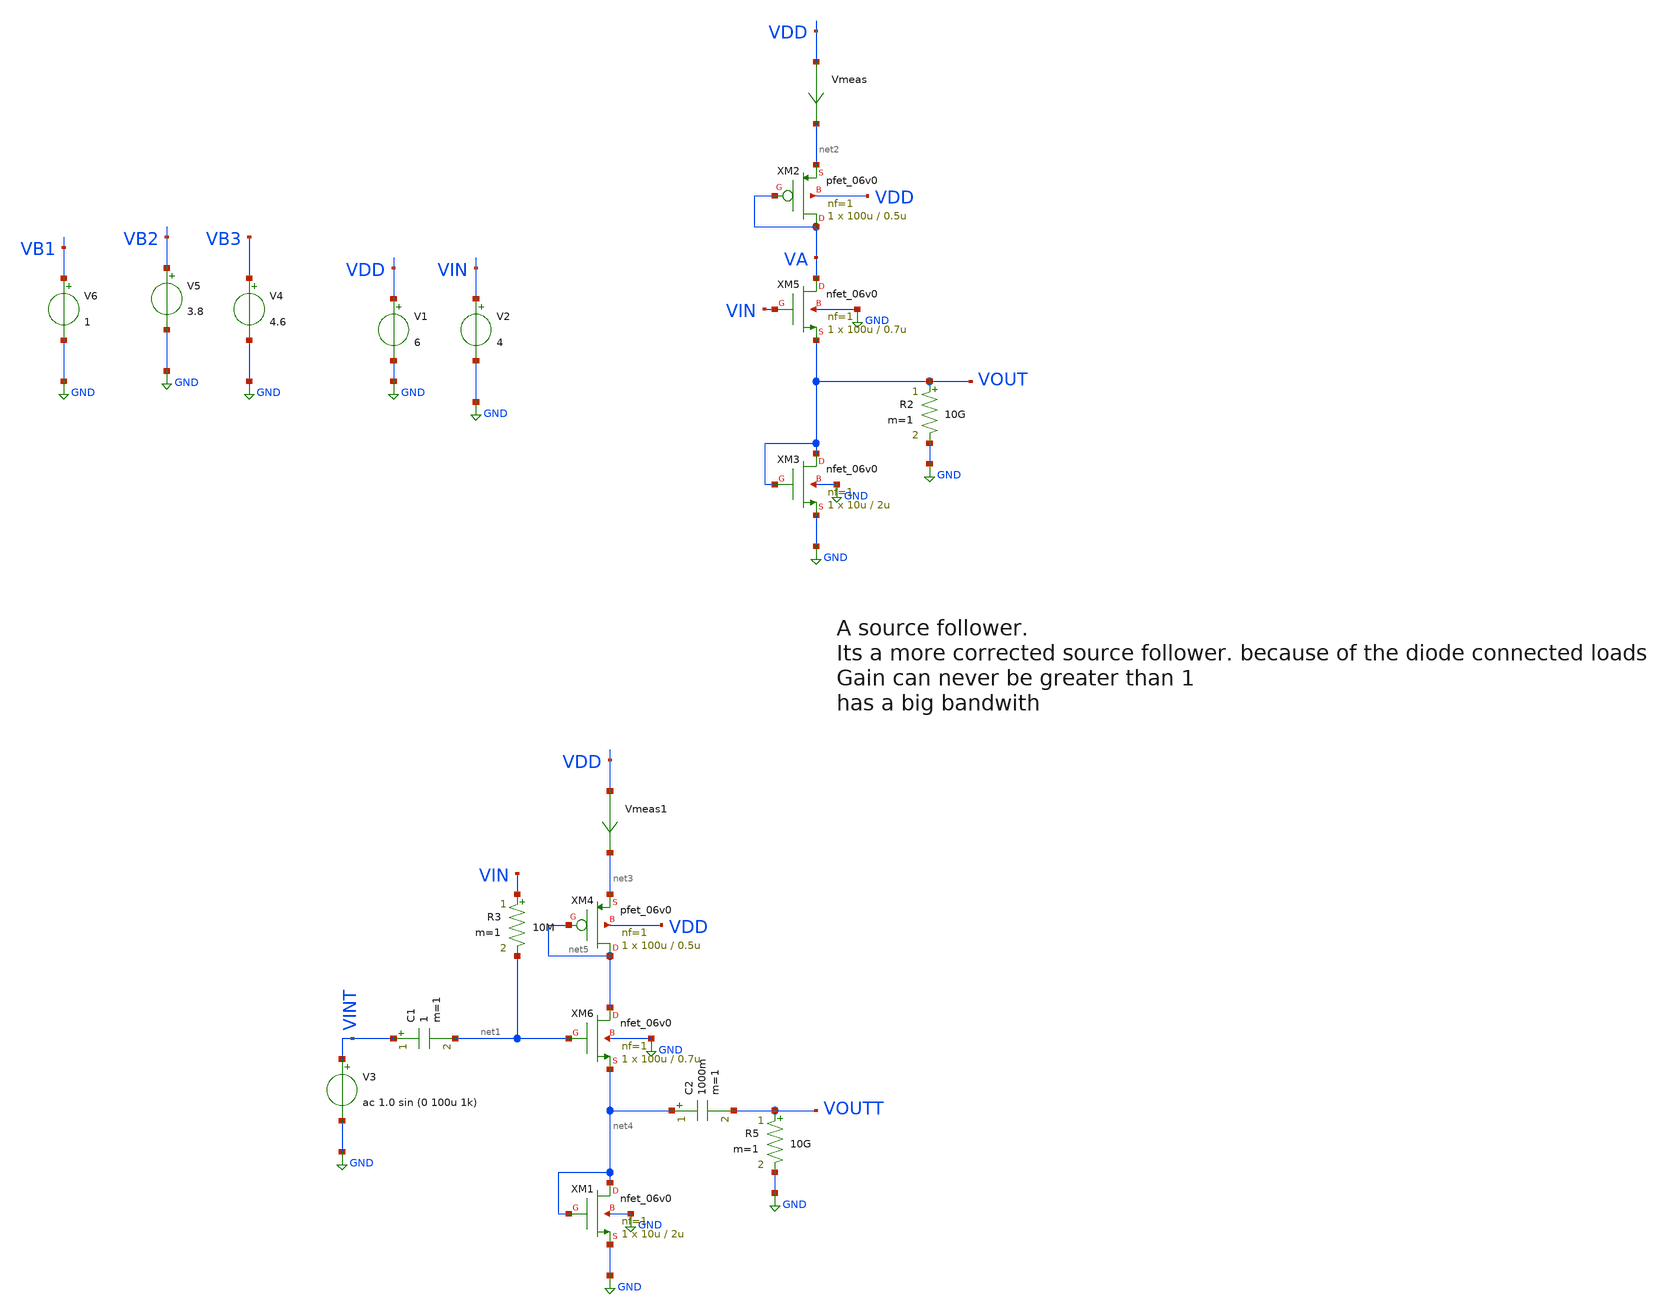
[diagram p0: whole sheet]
** sch_path: unusual_amplifiers/unusual_amp19.sch
**.subckt unusual_amp19
Vmeas VDD net2 0
.save i(vmeas)
V1 VDD GND 6
V2 VIN GND 4
V3 VINT GND ac 1.0 sin (0 100u 1k)
R2 VOUT GND 10G m=1
C1 VINT net1 1 m=1
R3 VIN net1 10M m=1
C2 net4 VOUTT 1000m m=1
R5 VOUTT GND 10G m=1
XM3 VOUT VOUT GND GND nfet_06v0 L=2u W=10u nf=1 ad='int((nf+1)/2) * W/nf * 0.18u' as='int((nf+2)/2) * W/nf * 0.18u'
+ pd='2*int((nf+1)/2) * (W/nf + 0.18u)' ps='2*int((nf+2)/2) * (W/nf + 0.18u)' nrd='0.18u / W' nrs='0.18u / W'
+ sa=0 sb=0 sd=0 m=1
XM2 VA VA net2 VDD pfet_06v0 L=0.5u W=100u nf=1 ad='int((nf+1)/2) * W/nf * 0.18u' as='int((nf+2)/2) * W/nf * 0.18u'
+ pd='2*int((nf+1)/2) * (W/nf + 0.18u)' ps='2*int((nf+2)/2) * (W/nf + 0.18u)' nrd='0.18u / W' nrs='0.18u / W'
+ sa=0 sb=0 sd=0 m=1
V4 VB3 GND 4.6
V5 VB2 GND 3.8
V6 VB1 GND 1
XM5 VA VIN VOUT GND nfet_06v0 L=0.7u W=100u nf=1 ad='int((nf+1)/2) * W/nf * 0.18u' as='int((nf+2)/2) * W/nf * 0.18u'
+ pd='2*int((nf+1)/2) * (W/nf + 0.18u)' ps='2*int((nf+2)/2) * (W/nf + 0.18u)' nrd='0.18u / W' nrs='0.18u / W'
+ sa=0 sb=0 sd=0 m=1
Vmeas1 VDD net3 0
.save i(vmeas1)
XM1 net4 net4 GND GND nfet_06v0 L=2u W=10u nf=1 ad='int((nf+1)/2) * W/nf * 0.18u' as='int((nf+2)/2) * W/nf * 0.18u'
+ pd='2*int((nf+1)/2) * (W/nf + 0.18u)' ps='2*int((nf+2)/2) * (W/nf + 0.18u)' nrd='0.18u / W' nrs='0.18u / W'
+ sa=0 sb=0 sd=0 m=1
XM4 net5 net5 net3 VDD pfet_06v0 L=0.5u W=100u nf=1 ad='int((nf+1)/2) * W/nf * 0.18u' as='int((nf+2)/2) * W/nf * 0.18u'
+ pd='2*int((nf+1)/2) * (W/nf + 0.18u)' ps='2*int((nf+2)/2) * (W/nf + 0.18u)' nrd='0.18u / W' nrs='0.18u / W'
+ sa=0 sb=0 sd=0 m=1
XM6 net5 net1 net4 GND nfet_06v0 L=0.7u W=100u nf=1 ad='int((nf+1)/2) * W/nf * 0.18u' as='int((nf+2)/2) * W/nf * 0.18u'
+ pd='2*int((nf+1)/2) * (W/nf + 0.18u)' ps='2*int((nf+2)/2) * (W/nf + 0.18u)' nrd='0.18u / W' nrs='0.18u / W'
+ sa=0 sb=0 sd=0 m=1
**** begin user architecture code

**************************************************************
**************************************************************
**************************************************************
**************************************************************
**************************************************************
*LIBs*********************************************************
**************************************************************
**************************************************************
**************************************************************
**************************************************************
**************************************************************
.include $::180MCU_MODELS/design.ngspice
*.lib $::180MCU_MODELS/sm141064.ngspice statistical *use statistical if you want global and parameter mismatch
*.lib $::180MCU_MODELS/sm141064.ngspice res_statistical
.lib $::180MCU_MODELS/sm141064.ngspice typical
.lib $::180MCU_MODELS/sm141064.ngspice res_typical
.lib $::180MCU_MODELS/sm141064.ngspice moscap_typical
.lib $::180MCU_MODELS/sm141064.ngspice bjt_typical
.lib $::180MCU_MODELS/sm141064.ngspice diode_typical
.lib $::180MCU_MODELS/sm141064.ngspice mimcap_typical
**************************************************************
**************************************************************
**************************************************************
**************************************************************
**************************************************************
*Corners/montecarlo options***********************************
**************************************************************
**************************************************************
**************************************************************
**************************************************************
**************************************************************
.TEMP 27
.param   sw_stat_global = 1   sw_stat_mism = 1  mc_skew = 3  res_mc_skew = 3  cap_mc_skew = 3
+  fnoicor = 1
**************************************************************
**************************************************************
**************************************************************
**************************************************************
*SIMULATION and Plots*****************************************
**************************************************************
**************************************************************
**************************************************************
**************************************************************
.control
save all
dc V2 0 6 0.01
*dc simulation
plot v(VOUT) v(VIN) deriv(v(VOUT)) v(VA)
*ploting VIN VOUT and the voltage gain
plot i(Vmeas)
*ploting the current for curiosity
tran 1us 2m
*transient simulation
plot (v(VINT)) (v(VOUTT))
*simple plot to exemplify the gain
fft v(VOUTT) v(VINT)
*fast fourier transfor
plot mag(v(VOUTT)) mag(v(VINT))
* analyse the frequency spectrum of the transient waves, to detect distortion
ac dec 20 1 50G
*simple ac simulation
plot v(VOUTT)
*gain in function of the input frequency
.endc

**** end user architecture code
**.ends
.GLOBAL GND
.end
